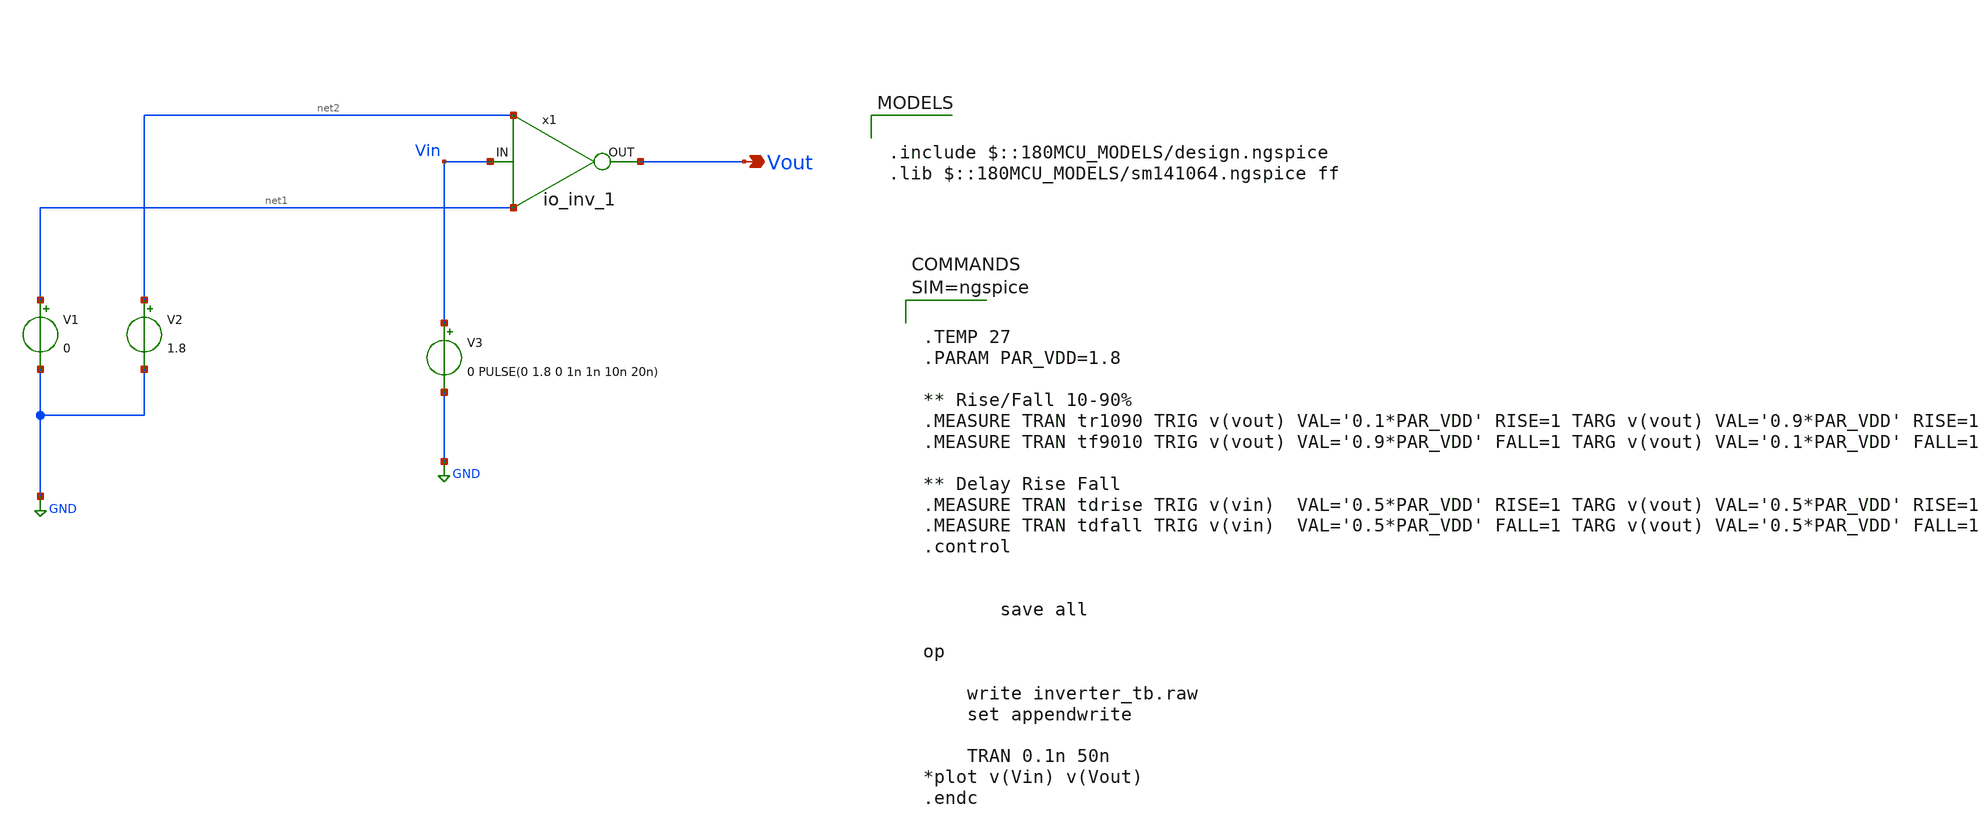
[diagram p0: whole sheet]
** sch_path: xschem/io_inv_1_tb.sch
* Copyright 2023 David Mitchell Bailey
* Licensed under the Apache License, Version 2.0 (the "License");
* you may not use this file except in compliance with the License.
* You may obtain a copy of the License at
* https://www.apache.org/licenses/LICENSE-2.0
* Unless required by applicable law or agreed to in writing, software
* distributed under the License is distributed on an "AS IS" BASIS,
* WITHOUT WARRANTIES OR CONDITIONS OF ANY KIND, either express or implied.
* See the License for the specific language governing permissions and
* limitations under the License.
**.subckt io_inv_1_tb Vout
*.opin Vout
x1 Vin Vout net2 net1 io_inv_1
V1 net1 GND 0
V2 net2 GND 1.8
V3 Vin GND 0 PULSE(0 1.8 0 1n 1n 10n 20n)
**** begin user architecture code

.include $::180MCU_MODELS/design.ngspice
.lib $::180MCU_MODELS/sm141064.ngspice ff




.TEMP 27
.PARAM PAR_VDD=1.8

** Rise/Fall 10-90%
.MEASURE TRAN tr1090 TRIG v(vout) VAL='0.1*PAR_VDD' RISE=1 TARG v(vout) VAL='0.9*PAR_VDD' RISE=1
.MEASURE TRAN tf9010 TRIG v(vout) VAL='0.9*PAR_VDD' FALL=1 TARG v(vout) VAL='0.1*PAR_VDD' FALL=1

** Delay Rise Fall
.MEASURE TRAN tdrise TRIG v(vin)  VAL='0.5*PAR_VDD' RISE=1 TARG v(vout) VAL='0.5*PAR_VDD' RISE=1
.MEASURE TRAN tdfall TRIG v(vin)  VAL='0.5*PAR_VDD' FALL=1 TARG v(vout) VAL='0.5*PAR_VDD' FALL=1
.control


	   save all

op

    write inverter_tb.raw
    set appendwrite

	TRAN 0.1n 50n
*plot v(Vin) v(Vout)
.endc




**** end user architecture code
**.ends
.GLOBAL GND
.end
